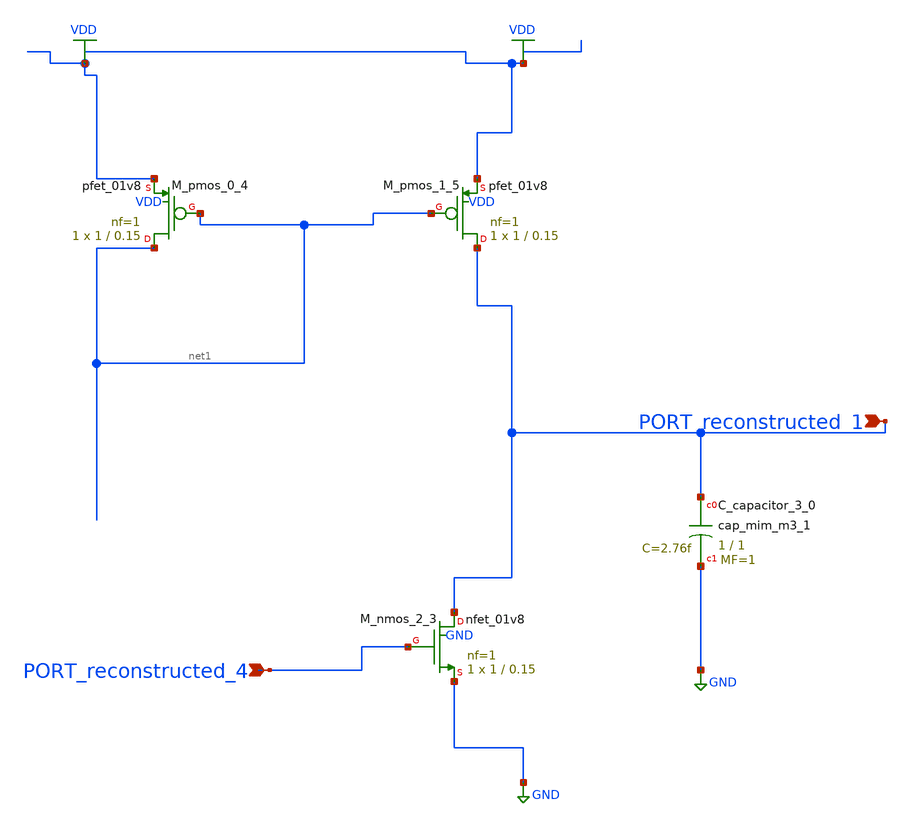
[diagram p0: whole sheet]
** sch_path: schematics/AMSNet/701.sch
**.subckt 701 PORT_reconstructed_4 PORT_reconstructed_1
*.ipin PORT_reconstructed_4
*.ipin PORT_reconstructed_1
XC_capacitor_3_0 PORT_reconstructed_1 GND sky130_fd_pr__cap_mim_m3_1 W=1 L=1 MF=1 m=1
XM_nmos_2_3 PORT_reconstructed_1 PORT_reconstructed_4 GND GND sky130_fd_pr__nfet_01v8 L=0.15 W=1 nf=1
+ ad='int((1 + 1)/2) * 1 / 1 * 0.29' as='int((1 + 2)/2) * 1 / 1 * 0.29' pd='2*int((1 + 1)/2) * (1 / 1 + 0.29)'
+ ps='2*int((1 + 2)/2) * (1 / 1 + 0.29)' nrd='0.29 / 1 ' nrs='0.29 / 1 ' sa=0 sb=0 sd=0 mult=1 m=1
XM_pmos_0_4 net1 net1 VDD VDD sky130_fd_pr__pfet_01v8 L=0.15 W=1 nf=1 ad='int((1 + 1)/2) * 1 / 1 * 0.29'
+ as='int((1 + 2)/2) * 1 / 1 * 0.29' pd='2*int((1 + 1)/2) * (1 / 1 + 0.29)' ps='2*int((1 + 2)/2) * (1 / 1 + 0.29)'
+ nrd='0.29 / 1 ' nrs='0.29 / 1 ' sa=0 sb=0 sd=0 mult=1 m=1
XM_pmos_1_5 PORT_reconstructed_1 net1 VDD VDD sky130_fd_pr__pfet_01v8 L=0.15 W=1 nf=1 ad='int((1 + 1)/2) * 1 / 1 * 0.29'
+ as='int((1 + 2)/2) * 1 / 1 * 0.29' pd='2*int((1 + 1)/2) * (1 / 1 + 0.29)' ps='2*int((1 + 2)/2) * (1 / 1 + 0.29)'
+ nrd='0.29 / 1 ' nrs='0.29 / 1 ' sa=0 sb=0 sd=0 mult=1 m=1
**.ends
.GLOBAL GND
.GLOBAL VDD
.end
